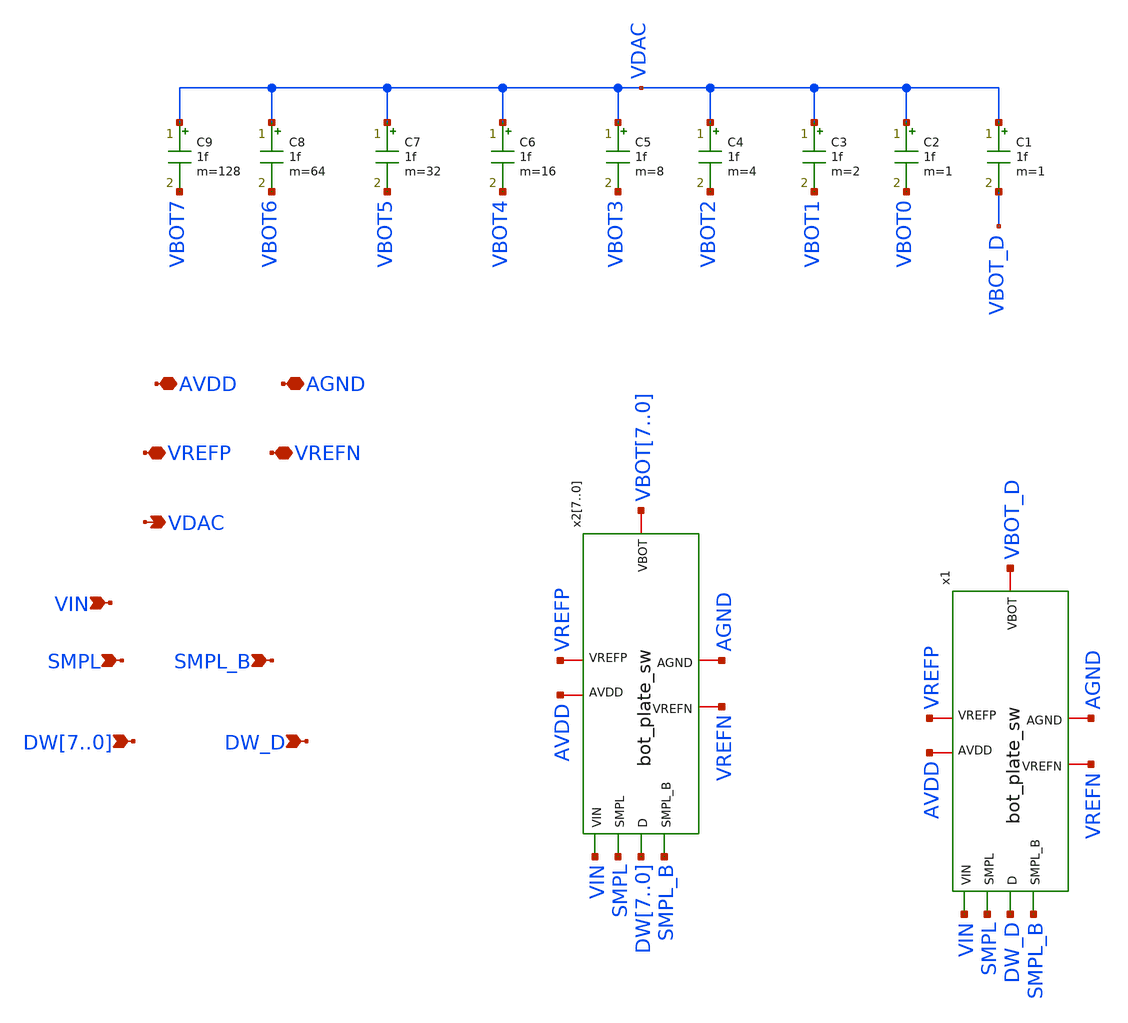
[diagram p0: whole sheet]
** sch_path: my_cac.sch
**.subckt my_cac AVDD AGND VREFP VREFN VIN SMPL SMPL_B DW7,DW6,DW5,DW4,DW3,DW2,DW1,DW0 DW_D VDAC
*.iopin AVDD
*.iopin AGND
*.iopin VREFP
*.iopin VREFN
*.ipin VIN
*.ipin SMPL
*.ipin SMPL_B
*.ipin DW7,DW6,DW5,DW4,DW3,DW2,DW1,DW0
*.ipin DW_D
*.opin VDAC
x1 AVDD AGND VBOT_D VREFN VREFP VIN SMPL DW_D SMPL_B bot_plate_sw
x27 AVDD AGND VBOT7 VREFN VREFP VIN SMPL DW7 SMPL_B bot_plate_sw
x26 AVDD AGND VBOT6 VREFN VREFP VIN SMPL DW6 SMPL_B bot_plate_sw
x25 AVDD AGND VBOT5 VREFN VREFP VIN SMPL DW5 SMPL_B bot_plate_sw
x24 AVDD AGND VBOT4 VREFN VREFP VIN SMPL DW4 SMPL_B bot_plate_sw
x23 AVDD AGND VBOT3 VREFN VREFP VIN SMPL DW3 SMPL_B bot_plate_sw
x22 AVDD AGND VBOT2 VREFN VREFP VIN SMPL DW2 SMPL_B bot_plate_sw
x21 AVDD AGND VBOT1 VREFN VREFP VIN SMPL DW1 SMPL_B bot_plate_sw
x20 AVDD AGND VBOT0 VREFN VREFP VIN SMPL DW0 SMPL_B bot_plate_sw
C1 VDAC VBOT_D 1f m=1
C2 VDAC VBOT0 1f m=1
C3 VDAC VBOT1 1f m=2
C4 VDAC VBOT2 1f m=4
C5 VDAC VBOT3 1f m=8
C6 VDAC VBOT4 1f m=16
C7 VDAC VBOT5 1f m=32
C8 VDAC VBOT6 1f m=64
C9 VDAC VBOT7 1f m=128
**.ends

* expanding   symbol:  bot_plate_sw.sym # of pins=9
** sym_path: bot_plate_sw.sym
** sch_path: bot_plate_sw.sch
.subckt bot_plate_sw AVDD AGND VBOT VREFN VREFP VIN SMPL D SMPL_B
*.iopin AVDD
*.iopin AGND
*.ipin VIN
*.ipin SMPL
*.iopin VREFN
*.iopin VREFP
*.ipin D
*.iopin VBOT
*.ipin SMPL_B
XM1 VBOT net2 VREFN AGND nfet_03v3 L=0.28u W=5u nf=1 ad='int((nf+1)/2) * W/nf * 0.18u' as='int((nf+2)/2) * W/nf * 0.18u'
+ pd='2*int((nf+1)/2) * (W/nf + 0.18u)' ps='2*int((nf+2)/2) * (W/nf + 0.18u)' nrd='0.18u / W' nrs='0.18u / W'
+ sa=0 sb=0 sd=0 m=1
XM2 VREFP net1 VBOT AVDD pfet_03v3 L=0.28u W=10u nf=1 ad='int((nf+1)/2) * W/nf * 0.18u' as='int((nf+2)/2) * W/nf * 0.18u'
+ pd='2*int((nf+1)/2) * (W/nf + 0.18u)' ps='2*int((nf+2)/2) * (W/nf + 0.18u)' nrd='0.18u / W' nrs='0.18u / W'
+ sa=0 sb=0 sd=0 m=1
x1 SMPL AGND VBOT VIN AVDD tg
x2 D net1 SMPL_B my_nand
x3 D net2 SMPL my_nor
.ends


* expanding   symbol:  tg.sym # of pins=5
** sym_path: tg.sym
** sch_path: tg.sch
.subckt tg EN AGND VOUT VIN AVDD
*.iopin AGND
*.iopin AVDD
*.iopin EN
*.iopin VOUT
*.iopin VIN
XM1 VOUT EN VIN AGND nfet_03v3 L=0.28u W=5u nf=1 ad='int((nf+1)/2) * W/nf * 0.18u' as='int((nf+2)/2) * W/nf * 0.18u'
+ pd='2*int((nf+1)/2) * (W/nf + 0.18u)' ps='2*int((nf+2)/2) * (W/nf + 0.18u)' nrd='0.18u / W' nrs='0.18u / W'
+ sa=0 sb=0 sd=0 m=1
XM2 VOUT ENB VIN AVDD pfet_03v3 L=0.28u W=10u nf=1 ad='int((nf+1)/2) * W/nf * 0.18u' as='int((nf+2)/2) * W/nf * 0.18u'
+ pd='2*int((nf+1)/2) * (W/nf + 0.18u)' ps='2*int((nf+2)/2) * (W/nf + 0.18u)' nrd='0.18u / W' nrs='0.18u / W'
+ sa=0 sb=0 sd=0 m=1
E1 ENB AVDD EN AGND -1
.ends


* expanding   symbol:  my_nand.sym # of pins=3
** sym_path: my_nand.sym
** sch_path: my_nand.sch
.subckt my_nand B Y A
*.ipin B
*.ipin A
*.opin Y
**** begin user architecture code

a6 [A B] Yi nand1
.model nand1 d_nand(rise_delay = 1e-9 fall_delay = 1e-9 input_load = 1e-12)

v1 Yi Y 0


**** end user architecture code
.ends


* expanding   symbol:  my_nor.sym # of pins=3
** sym_path: my_nor.sym
** sch_path: my_nor.sch
.subckt my_nor B Y A
*.ipin B
*.ipin A
*.opin Y
**** begin user architecture code

a6 [A B] Yi nor1
.model nor1 d_nor(rise_delay = 1e-9 fall_delay = 1e-9 input_load = 1e-12)

v1 Yi Y 0


**** end user architecture code
.ends

.end
